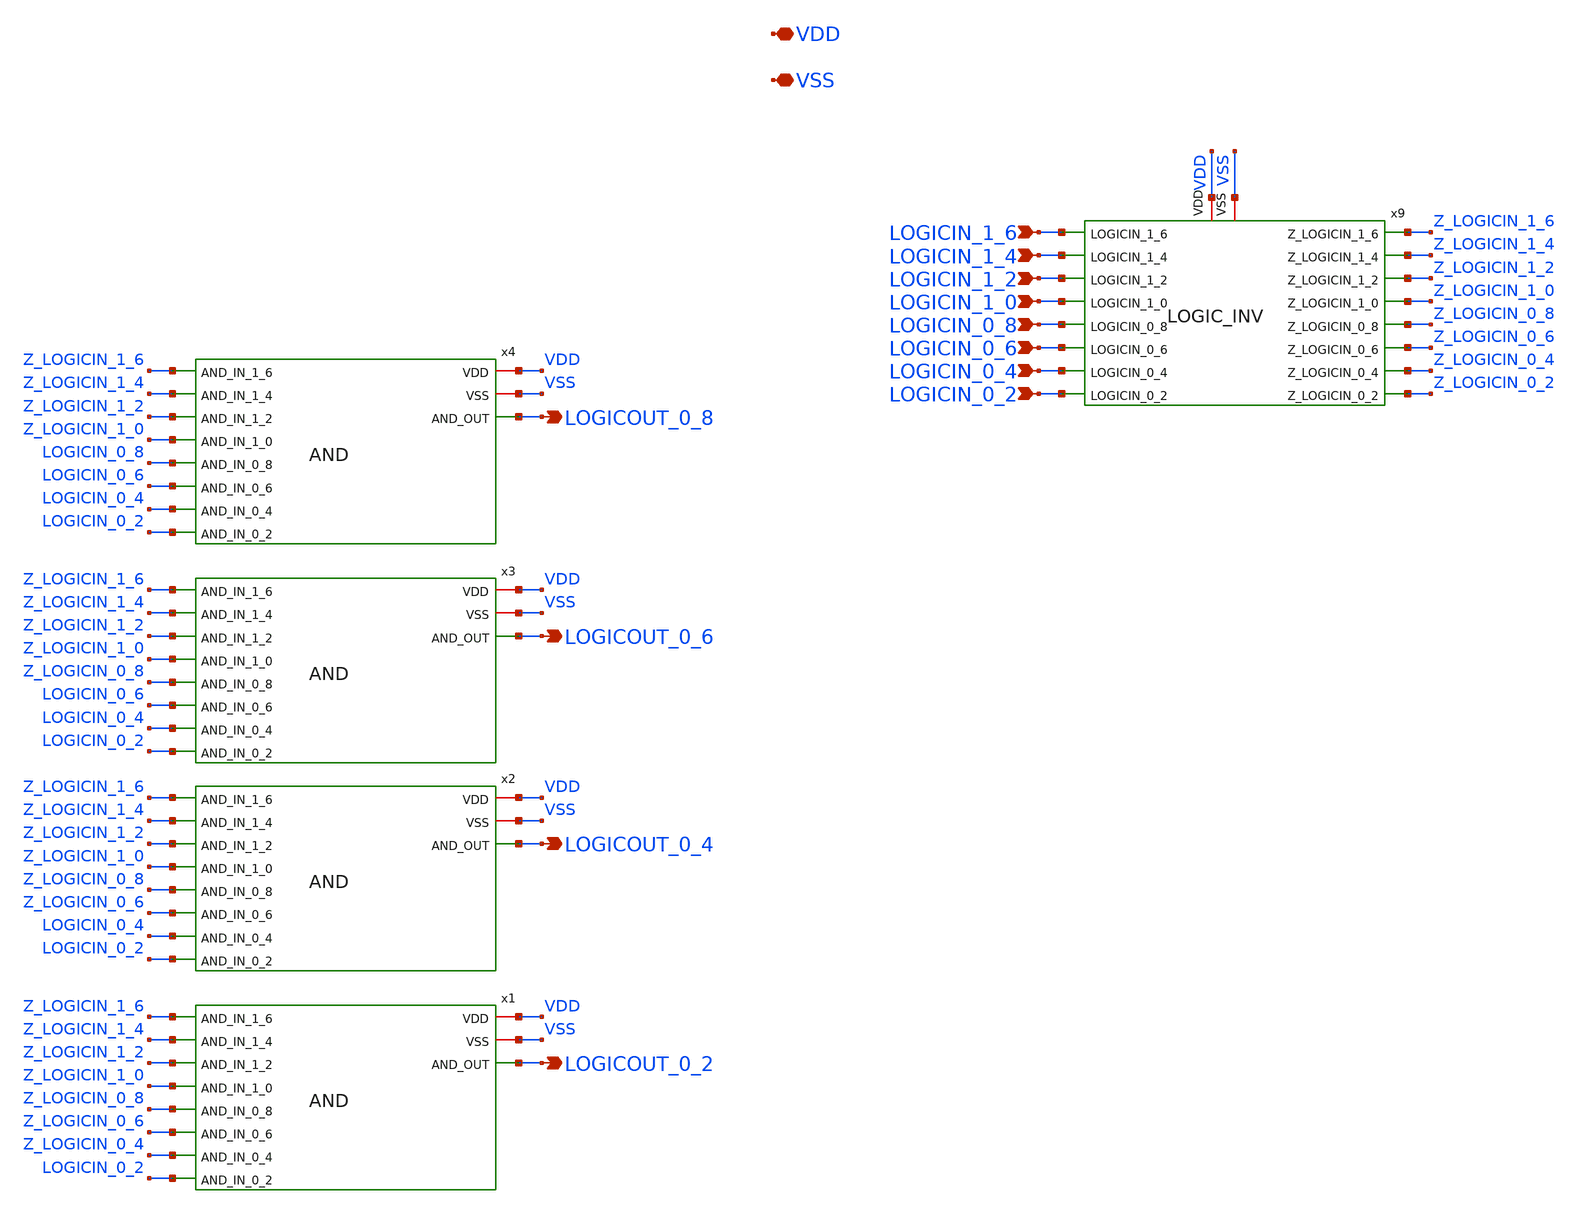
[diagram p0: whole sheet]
** sch_path: xschem/LOGIC_fix3.sch
**.subckt LOGIC_fix3 LOGICOUT_0_2 LOGICOUT_0_4 LOGICOUT_0_6 LOGICOUT_0_8 LOGICIN_1_0 LOGICIN_1_2
*+ LOGICIN_1_4 LOGICIN_1_6 LOGICIN_0_2 LOGICIN_0_4 LOGICIN_0_6 LOGICIN_0_8 VDD VSS
*.opin LOGICOUT_0_2
*.opin LOGICOUT_0_4
*.opin LOGICOUT_0_6
*.opin LOGICOUT_0_8
*.ipin LOGICIN_1_0
*.ipin LOGICIN_1_2
*.ipin LOGICIN_1_4
*.ipin LOGICIN_1_6
*.ipin LOGICIN_0_2
*.ipin LOGICIN_0_4
*.ipin LOGICIN_0_6
*.ipin LOGICIN_0_8
*.iopin VDD
*.iopin VSS
x1 VDD VSS Z_LOGICIN_1_6 Z_LOGICIN_1_4 Z_LOGICIN_1_2 Z_LOGICIN_1_0 LOGICOUT_0_2 Z_LOGICIN_0_8
+ Z_LOGICIN_0_6 Z_LOGICIN_0_4 LOGICIN_0_2 AND
x2 VDD VSS Z_LOGICIN_1_6 Z_LOGICIN_1_4 Z_LOGICIN_1_2 Z_LOGICIN_1_0 LOGICOUT_0_4 Z_LOGICIN_0_8
+ Z_LOGICIN_0_6 LOGICIN_0_4 LOGICIN_0_2 AND
x3 VDD VSS Z_LOGICIN_1_6 Z_LOGICIN_1_4 Z_LOGICIN_1_2 Z_LOGICIN_1_0 LOGICOUT_0_6 Z_LOGICIN_0_8
+ LOGICIN_0_6 LOGICIN_0_4 LOGICIN_0_2 AND
x4 VDD VSS Z_LOGICIN_1_6 Z_LOGICIN_1_4 Z_LOGICIN_1_2 Z_LOGICIN_1_0 LOGICOUT_0_8 LOGICIN_0_8
+ LOGICIN_0_6 LOGICIN_0_4 LOGICIN_0_2 AND
x9 LOGICIN_1_6 Z_LOGICIN_1_6 Z_LOGICIN_1_4 LOGICIN_1_4 LOGICIN_1_2 Z_LOGICIN_1_2 LOGICIN_1_0
+ Z_LOGICIN_1_0 Z_LOGICIN_0_8 LOGICIN_0_8 Z_LOGICIN_0_6 LOGICIN_0_6 LOGICIN_0_4 Z_LOGICIN_0_4 LOGICIN_0_2
+ Z_LOGICIN_0_2 VDD VSS LOGIC_INV
**.ends
.end
